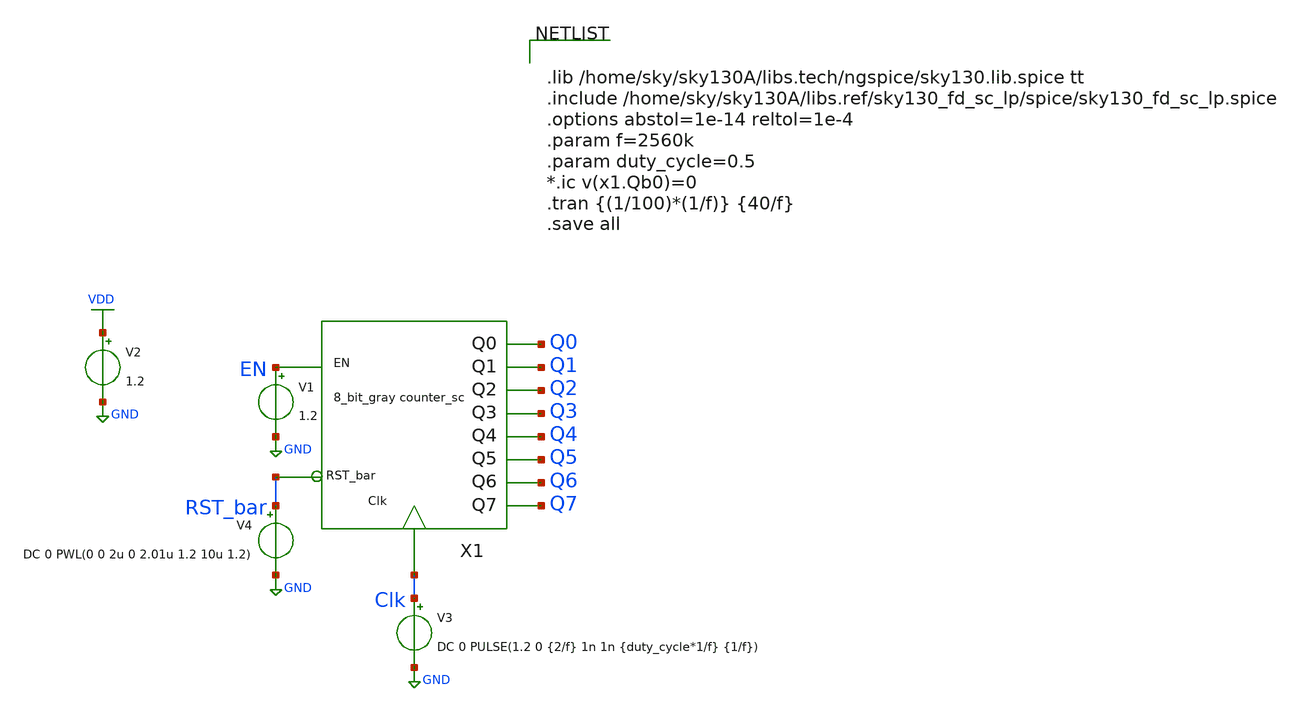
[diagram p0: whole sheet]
** sch_path: xschem/Asyn_rst_gray_counter/asyn_rst_gray_counter_tb.sch
**.subckt asyn_rst_gray_counter_tb
V3 Clk GND DC 0 PULSE(1.2 0 {2/f} 1n 1n {duty_cycle*1/f} {1/f})
V1 EN GND 1.2
V2 VDD GND 1.2
X1 EN Q1 Q6 Clk Q0 Q2 Q3 Q4 Q5 Q7 RST_bar asyn_rst_gray_counter
V4 RST_bar GND DC 0 PWL(0 0 2u 0 2.01u 1.2 10u 1.2)
**** begin user architecture code


.lib /home/sky/sky130A/libs.tech/ngspice/sky130.lib.spice tt
.include /home/sky/sky130A/libs.ref/sky130_fd_sc_lp/spice/sky130_fd_sc_lp.spice
.options abstol=1e-14 reltol=1e-4
.param f=2560k
.param duty_cycle=0.5
*.ic v(x1.Qb0)=0
.tran {(1/100)*(1/f)} {40/f}
.save all


**** end user architecture code
**.ends

* expanding   symbol:  Asyn_rst_gray_counter/asyn_rst_gray_counter.sym # of pins=11
** sym_path: Asyn_rst_gray_counter/asyn_rst_gray_counter.sym
** sch_path: Asyn_rst_gray_counter/asyn_rst_gray_counter.sch
.subckt asyn_rst_gray_counter EN Q1 Q6 Clk Q0 Q2 Q3 Q4 Q5 Q7 RST_bar
*.ipin Clk
*.ipin EN
*.opin Q0
*.opin Q1
*.opin Q2
*.opin Q4
*.opin Q5
*.opin Q6
*.opin Q7
*.opin Q3
*.ipin RST_bar
x14 qb1 qb0 GND GND VDD VDD Q0 sky130_fd_sc_lp__xor2_1
x15 net1 qb1 GND GND VDD VDD net2 sky130_fd_sc_lp__and2_1
x1 qb2 qb1 GND GND VDD VDD Q1 sky130_fd_sc_lp__xor2_1
x2 qb3 qb2 GND GND VDD VDD Q2 sky130_fd_sc_lp__xor2_1
x3 qb4 qb3 GND GND VDD VDD Q3 sky130_fd_sc_lp__xor2_1
x4 qb5 qb4 GND GND VDD VDD Q4 sky130_fd_sc_lp__xor2_1
x5 qb6 qb5 GND GND VDD VDD Q5 sky130_fd_sc_lp__xor2_1
x6 Q7 qb6 GND GND VDD VDD Q6 sky130_fd_sc_lp__xor2_1
x7 net2 qb2 GND GND VDD VDD net3 sky130_fd_sc_lp__and2_1
x8 net4 qb4 GND GND VDD VDD net5 sky130_fd_sc_lp__and2_1
x9 net3 qb3 GND GND VDD VDD net4 sky130_fd_sc_lp__and2_1
x10 net5 qb5 GND GND VDD VDD net6 sky130_fd_sc_lp__and2_1
x11 net6 qb6 GND GND VDD VDD net7 sky130_fd_sc_lp__and2_1
x12 EN qb0 GND GND VDD VDD net1 sky130_fd_sc_lp__and2_1
X1 EN qb0 Clk RST_bar net8 net9 asyn_rst_t_ff
X2 net1 qb1 Clk RST_bar net10 net11 asyn_rst_t_ff
X3 net2 qb2 Clk RST_bar net12 net13 asyn_rst_t_ff
X4 net3 qb3 Clk RST_bar net14 net15 asyn_rst_t_ff
X5 net4 qb4 Clk RST_bar net16 net17 asyn_rst_t_ff
X6 net5 qb5 Clk RST_bar net18 net19 asyn_rst_t_ff
X7 net6 qb6 Clk RST_bar net20 net21 asyn_rst_t_ff
X8 net7 Q7 Clk RST_bar net22 net23 asyn_rst_t_ff
.ends


* expanding   symbol:  T_flip_flop/asyn_rst_t_ff.sym # of pins=6
** sym_path: xschem/T_flip_flop/asyn_rst_t_ff.sym
** sch_path: xschem/T_flip_flop/asyn_rst_t_ff.sch
.subckt asyn_rst_t_ff T Q CLK RST_bar GND VDD
*.ipin T
*.ipin CLK
*.opin Q
*.ipin RST_bar
*.iopin VDD
*.iopin GND
x1 CLK net1 RST_bar GND GND VDD VDD Q sky130_fd_sc_lp__dfrtp_1
x3 T Q GND GND VDD VDD net1 sky130_fd_sc_lp__xor2_1
.ends

.GLOBAL GND
.GLOBAL VDD
.end
